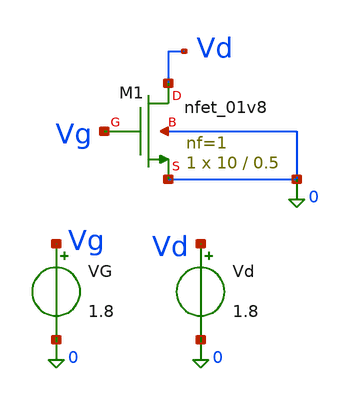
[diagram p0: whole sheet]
** sch_path: characterization/Schematics/nmos_characterization.sch
**.subckt nmos_characterization
VG Vg 0 1.8
Vd Vd 0 1.8
XM1 Vd Vg 0 0 sky130_fd_pr__nfet_01v8 L=0.5 W=10 nf=1 ad='int((1 + 1)/2) * 10 / 1 * 0.29' as='int((1 + 2)/2) * 10 / 1 * 0.29'
+ pd='2*int((1 + 1)/2) * (10 / 1 + 0.29)' ps='2*int((1 + 2)/2) * (10 / 1 + 0.29)' nrd='0.29 / 10 ' nrs='0.29 / 10 '
+ sa=0 sb=0 sd=0 mult=1 m=1
**** begin user architecture code

** opencircuitdesign pdks install
.lib $::SKYWATER_MODELS/sky130.lib.spice tt


.options savecurrents

.control
    save all

    * =====================================================
    * NMOS gm/Id characterization
    * VS = VB = 0 V
    * W = 10 um
    * L = 0.5 um
    * =====================================================

    * CASE 1: VDS = 1.8 V
    alter Vd 1.8
    dc Vg 0 1.8 0.001

    let id = abs(Vd#branch)
    let gm = deriv(id)
    let gm_id = gm / id
    let id_w = id / 10e-6


    * CASE 2: VDS = 0.9 V
    alter Vd 0.9
    dc Vg 0 1.8 0.001

    let id = abs(Vd#branch)
    let gm = deriv(id)
    let gm_id = gm / id
    let id_w = id / 10e-6


    * CASE 3: VDS = 0.6 V
    alter Vd 0.6
    dc Vg 0 1.8 0.001

    let id = abs(Vd#branch)
    let gm = deriv(id)
    let gm_id = gm / id
    let id_w = id / 10e-6


    * CASE 4: VDS = 0.3 V
    alter Vd 0.3
    dc Vg 0 1.8 0.001

    let id = abs(Vd#branch)
    let gm = deriv(id)
    let gm_id = gm / id
    let id_w = id / 10e-6


    * =====================================================
    * Copy results to const for friendly legend names
    * =====================================================

    setplot const

    let vds_1v8 = dc1.gm_id
    let idw_1v8 = dc1.id_w

    let vds_0v9 = dc2.gm_id
    let idw_0v9 = dc2.id_w

    let vds_0v6 = dc3.gm_id
    let idw_0v6 = dc3.id_w

    let vds_0v3 = dc4.gm_id
    let idw_0v3 = dc4.id_w


    * IMPORTANT: keep this plot command on ONE LINE
    plot vds_1v8 vs idw_1v8 vds_0v9 vs idw_0v9 vds_0v6 vs idw_0v6 vds_0v3 vs idw_0v3 xlog xlabel 'Id/W [uA/um]'
+ ylabel 'gm/Id [1/V]' title 'NMOS gm/Id Characterization'

.endc

**** end user architecture code
**.ends
.end
